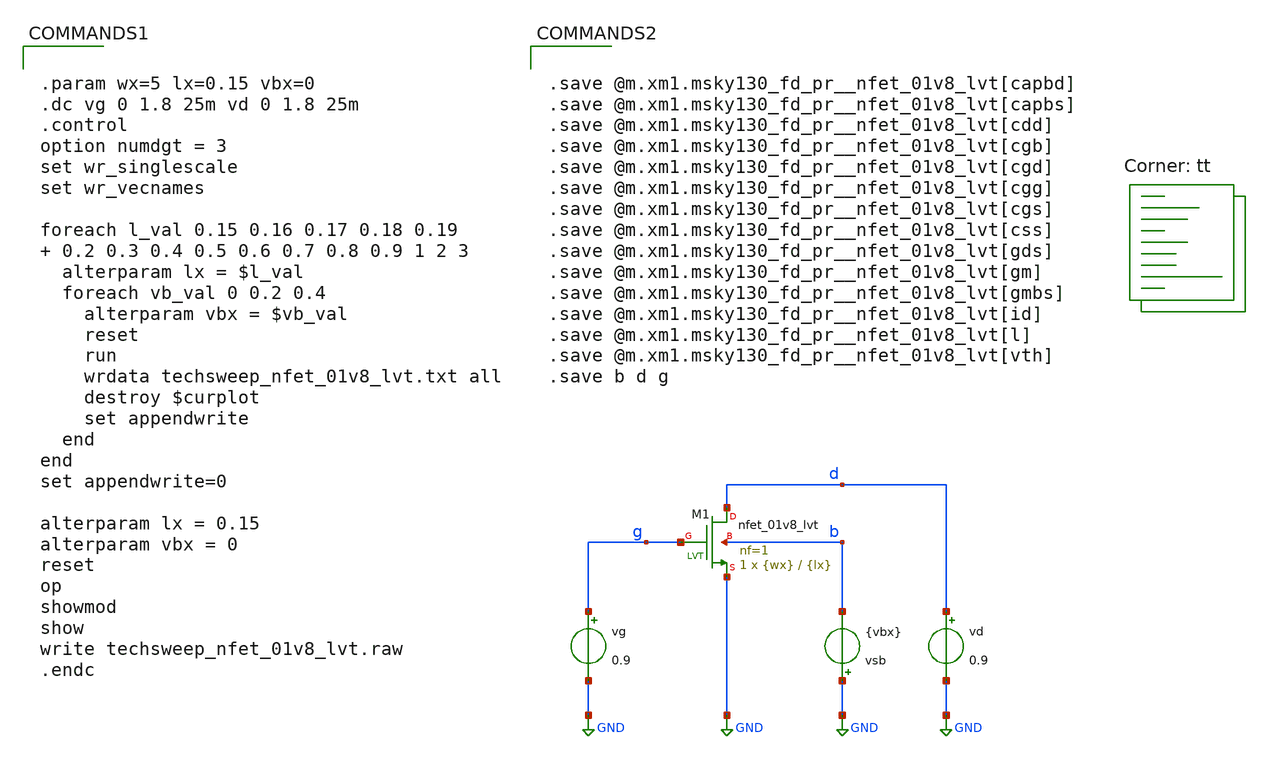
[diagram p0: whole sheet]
** sch_path: techsweep_nfet_01v8_lvt.sch
**.subckt techsweep_nfet_01v8_lvt
vg g GND 0.9
vd d GND 0.9
vsb GND b {vbx}
XM1 d g GND b sky130_fd_pr__nfet_01v8_lvt L={lx} W={wx} nf=1 ad='int((nf+1)/2) * W/nf * 0.29' as='int((nf+2)/2) * W/nf * 0.29'
+ pd='2*int((nf+1)/2) * (W/nf + 0.29)' ps='2*int((nf+2)/2) * (W/nf + 0.29)' nrd='0.29 / W' nrs='0.29 / W'
+ sa=0 sb=0 sd=0 mult=1 m=1
**** begin user architecture code


.param wx=5 lx=0.15 vbx=0
.dc vg 0 1.8 25m vd 0 1.8 25m
.control
option numdgt = 3
set wr_singlescale
set wr_vecnames

foreach l_val 0.15 0.16 0.17 0.18 0.19  0.2 0.3 0.4 0.5 0.6 0.7 0.8 0.9 1 2 3
  alterparam lx = $l_val
  foreach vb_val 0 0.2 0.4
    alterparam vbx = $vb_val
    reset
    run
    wrdata techsweep_nfet_01v8_lvt.txt all
    destroy $curplot
    set appendwrite
  end
end
set appendwrite=0

alterparam lx = 0.15
alterparam vbx = 0
reset
op
showmod
show
write techsweep_nfet_01v8_lvt.raw
.endc


.lib $::SKYWATER_MODELS/sky130.lib.spice tt


.save @m.xm1.msky130_fd_pr__nfet_01v8_lvt[capbd]
.save @m.xm1.msky130_fd_pr__nfet_01v8_lvt[capbs]
.save @m.xm1.msky130_fd_pr__nfet_01v8_lvt[cdd]
.save @m.xm1.msky130_fd_pr__nfet_01v8_lvt[cgb]
.save @m.xm1.msky130_fd_pr__nfet_01v8_lvt[cgd]
.save @m.xm1.msky130_fd_pr__nfet_01v8_lvt[cgg]
.save @m.xm1.msky130_fd_pr__nfet_01v8_lvt[cgs]
.save @m.xm1.msky130_fd_pr__nfet_01v8_lvt[css]
.save @m.xm1.msky130_fd_pr__nfet_01v8_lvt[gds]
.save @m.xm1.msky130_fd_pr__nfet_01v8_lvt[gm]
.save @m.xm1.msky130_fd_pr__nfet_01v8_lvt[gmbs]
.save @m.xm1.msky130_fd_pr__nfet_01v8_lvt[id]
.save @m.xm1.msky130_fd_pr__nfet_01v8_lvt[l]
.save @m.xm1.msky130_fd_pr__nfet_01v8_lvt[vth]
.save b d g


**** end user architecture code
**.ends
.GLOBAL GND
.end
